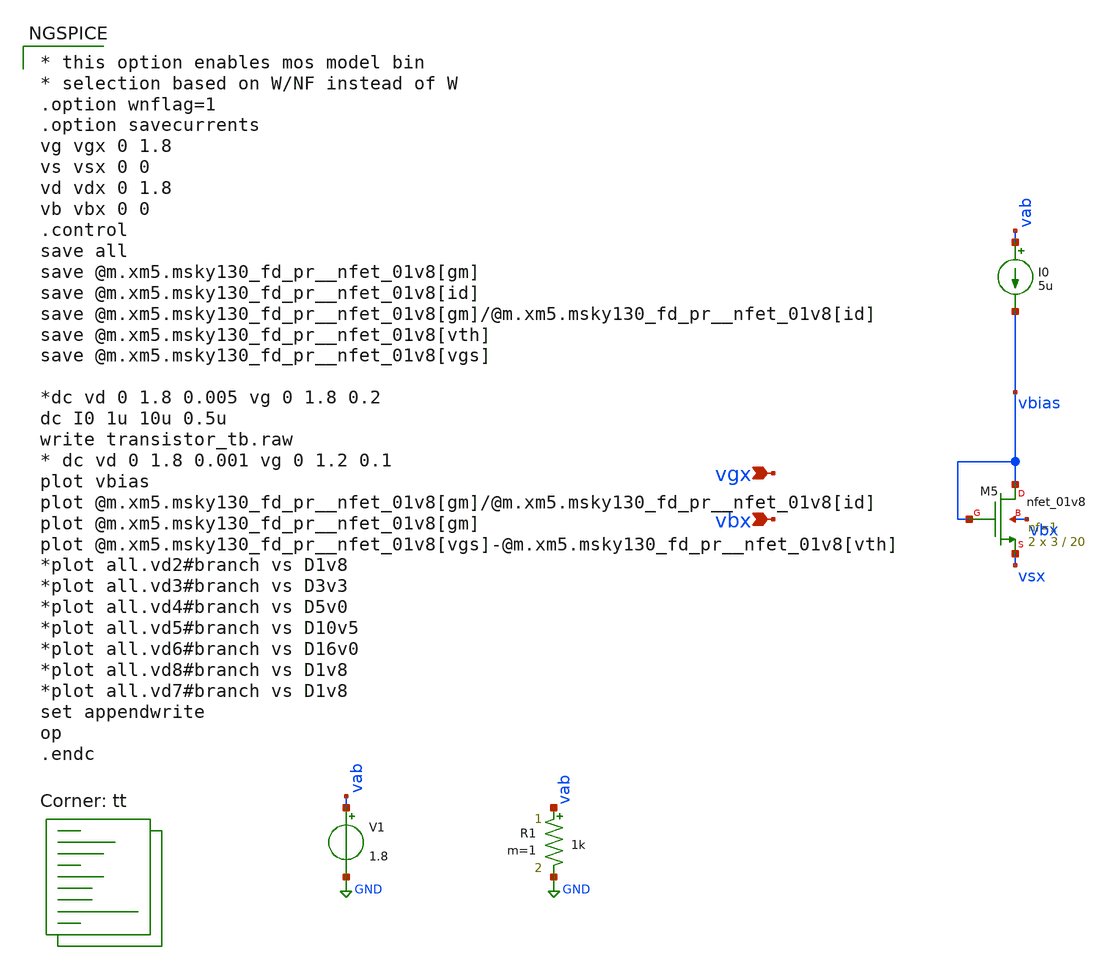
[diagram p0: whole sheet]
** sch_path: top/test/testbench/transistor_tb.sch
**.subckt transistor_tb vgx vbx
*.ipin vgx
*.ipin vbx
XM5 vbias vbias vsx vbx sky130_fd_pr__nfet_01v8 L=20 W=3 nf=1 ad='int((nf+1)/2) * W/nf * 0.29' as='int((nf+2)/2) * W/nf * 0.29'
+ pd='2*int((nf+1)/2) * (W/nf + 0.29)' ps='2*int((nf+2)/2) * (W/nf + 0.29)' nrd='0.29 / W' nrs='0.29 / W'
+ sa=0 sb=0 sd=0 mult=2 m=2
V1 vab GND 1.8
R1 vab GND 1k m=1
I0 vab vbias 5u
**** begin user architecture code

* this option enables mos model bin
* selection based on W/NF instead of W
.option wnflag=1
.option savecurrents
vg vgx 0 1.8
vs vsx 0 0
vd vdx 0 1.8
vb vbx 0 0
.control
save all
save @m.xm5.msky130_fd_pr__nfet_01v8[gm]
save @m.xm5.msky130_fd_pr__nfet_01v8[id]
save @m.xm5.msky130_fd_pr__nfet_01v8[gm]/@m.xm5.msky130_fd_pr__nfet_01v8[id]
save @m.xm5.msky130_fd_pr__nfet_01v8[vth]
save @m.xm5.msky130_fd_pr__nfet_01v8[vgs]

*dc vd 0 1.8 0.005 vg 0 1.8 0.2
dc I0 1u 10u 0.5u
write transistor_tb.raw
* dc vd 0 1.8 0.001 vg 0 1.2 0.1
plot vbias
plot @m.xm5.msky130_fd_pr__nfet_01v8[gm]/@m.xm5.msky130_fd_pr__nfet_01v8[id]
plot @m.xm5.msky130_fd_pr__nfet_01v8[gm]
plot @m.xm5.msky130_fd_pr__nfet_01v8[vgs]-@m.xm5.msky130_fd_pr__nfet_01v8[vth]
*plot all.vd2#branch vs D1v8
*plot all.vd3#branch vs D3v3
*plot all.vd4#branch vs D5v0
*plot all.vd5#branch vs D10v5
*plot all.vd6#branch vs D16v0
*plot all.vd8#branch vs D1v8
*plot all.vd7#branch vs D1v8
set appendwrite
op
.endc


.lib $::SKYWATER_MODELS/sky130.lib.spice tt
**** end user architecture code
**.ends
.GLOBAL GND
.end
